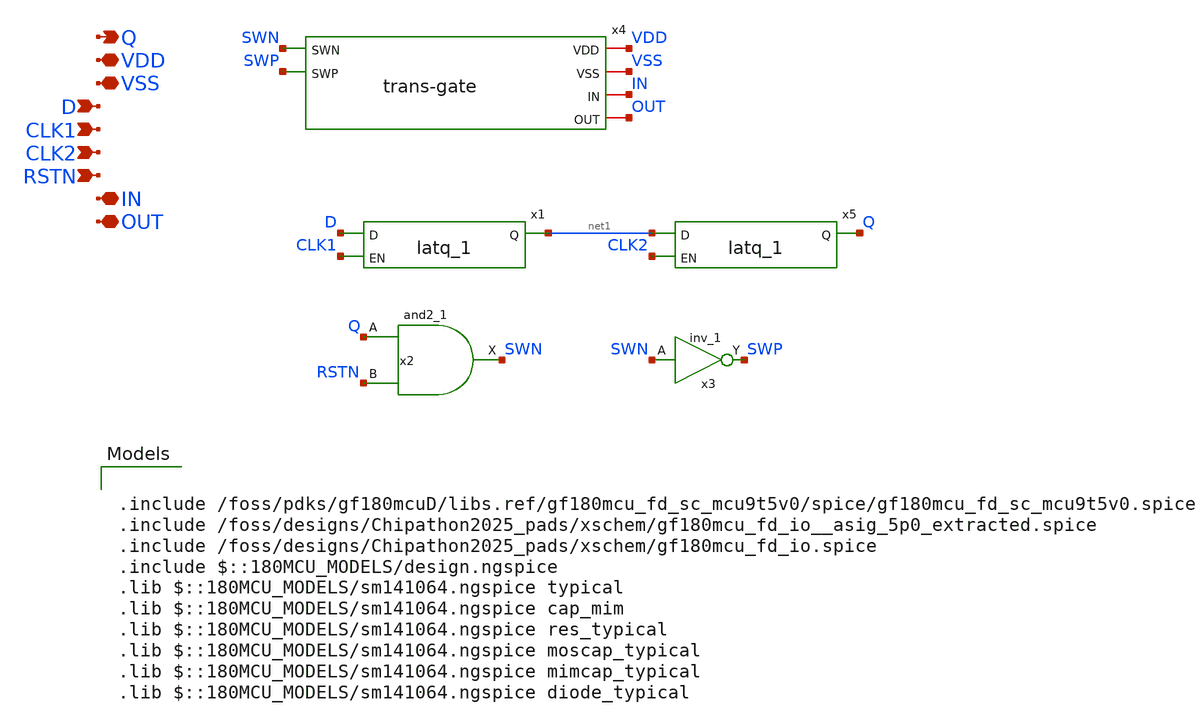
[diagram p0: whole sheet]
** sch_path: designs/libs/core_switch-matrix/switch-cell/switch-cell.sch
**.subckt switch-cell VDD VSS CLK1 D IN OUT RSTN Q CLK2
*.iopin VDD
*.iopin VSS
*.ipin CLK1
*.ipin D
*.iopin IN
*.iopin OUT
*.ipin RSTN
*.opin Q
*.ipin CLK2
x4 VDD VSS SWN SWP IN OUT trans-gate
x1 D CLK1 net1 VDD VDD VSS VSS gf180mcu_fd_sc_mcu9t5v0__latq_1
x5 net1 CLK2 Q VDD VDD VSS VSS gf180mcu_fd_sc_mcu9t5v0__latq_1
x2 Q RSTN VSS VDD VSS VDD SWN gf180mcu_fd_sc_mcu9t5v0__and2_1
x3 SWN VSS VDD VSS VDD SWP gf180mcu_fd_sc_mcu9t5v0__inv_1
**** begin user architecture code

.include /foss/pdks/gf180mcuD/libs.ref/gf180mcu_fd_sc_mcu9t5v0/spice/gf180mcu_fd_sc_mcu9t5v0.spice
.include /foss/designs/Chipathon2025_pads/xschem/gf180mcu_fd_io__asig_5p0_extracted.spice
.include /foss/designs/Chipathon2025_pads/xschem/gf180mcu_fd_io.spice
.include $::180MCU_MODELS/design.ngspice
.lib $::180MCU_MODELS/sm141064.ngspice typical
.lib $::180MCU_MODELS/sm141064.ngspice cap_mim
.lib $::180MCU_MODELS/sm141064.ngspice res_typical
.lib $::180MCU_MODELS/sm141064.ngspice moscap_typical
.lib $::180MCU_MODELS/sm141064.ngspice mimcap_typical
.lib $::180MCU_MODELS/sm141064.ngspice diode_typical

**** end user architecture code
**.ends

* expanding   symbol:  core_switch-matrix/trans-gate/trans-gate.sym # of pins=6
** sym_path: designs/libs/core_switch-matrix/trans-gate/trans-gate.sym
** sch_path: designs/libs/core_switch-matrix/trans-gate/trans-gate.sch
.subckt trans-gate VDD VSS SWN SWP IN OUT
*.iopin VDD
*.iopin VSS
*.iopin IN
*.iopin OUT
*.ipin SWN
*.ipin SWP
XM1 IN SWN OUT VSS nfet_06v0 L=0.70u W=8u nf=1 ad='int((nf+1)/2) * W/nf * 0.18u' as='int((nf+2)/2) * W/nf * 0.18u'
+ pd='2*int((nf+1)/2) * (W/nf + 0.18u)' ps='2*int((nf+2)/2) * (W/nf + 0.18u)' nrd='0.18u / W' nrs='0.18u / W'
+ sa=0 sb=0 sd=0 m=3
XM2 IN SWP OUT VDD pfet_06v0 L=0.55u W=8u nf=1 ad='int((nf+1)/2) * W/nf * 0.18u' as='int((nf+2)/2) * W/nf * 0.18u'
+ pd='2*int((nf+1)/2) * (W/nf + 0.18u)' ps='2*int((nf+2)/2) * (W/nf + 0.18u)' nrd='0.18u / W' nrs='0.18u / W'
+ sa=0 sb=0 sd=0 m=9
.ends

.end
